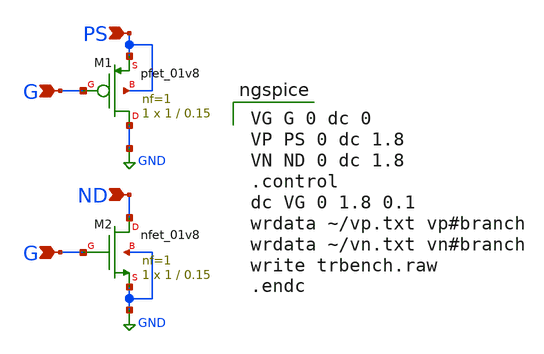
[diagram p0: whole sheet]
** sch_path: trbench.sch
**.subckt trbench ND PS G G
*.ipin ND
*.ipin PS
*.ipin G
*.ipin G
XM1 GND G PS PS sky130_fd_pr__pfet_01v8 L=0.15 W=1 nf=1 ad='int((nf+1)/2) * W/nf * 0.29' as='int((nf+2)/2) * W/nf * 0.29'
+ pd='2*int((nf+1)/2) * (W/nf + 0.29)' ps='2*int((nf+2)/2) * (W/nf + 0.29)' nrd='0.29 / W' nrs='0.29 / W'
+ sa=0 sb=0 sd=0 mult=1 m=1
XM2 ND G GND GND sky130_fd_pr__nfet_01v8 L=0.15 W=1 nf=1 ad='int((nf+1)/2) * W/nf * 0.29' as='int((nf+2)/2) * W/nf * 0.29'
+ pd='2*int((nf+1)/2) * (W/nf + 0.29)' ps='2*int((nf+2)/2) * (W/nf + 0.29)' nrd='0.29 / W' nrs='0.29 / W'
+ sa=0 sb=0 sd=0 mult=1 m=1
**** begin user architecture code

VG G 0 dc 0
VP PS 0 dc 1.8
VN ND 0 dc 1.8
.control
dc VG 0 1.8 0.1
wrdata ~/vp.txt vp#branch
wrdata ~/vn.txt vn#branch
write trbench.raw
.endc


** opencircuitdesign pdks install
.lib $::SKYWATER_MODELS/sky130.lib.spice tt


**** end user architecture code
**.ends
.GLOBAL GND
.end
